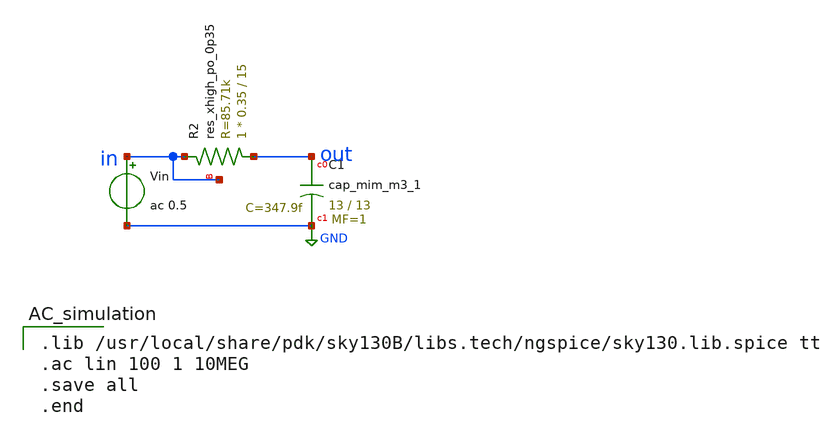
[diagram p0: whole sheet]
** sch_path: xschem/analog_desing/Filtro/LowPassFilter.sch
**.subckt LowPassFilter
XC1 out GND sky130_fd_pr__cap_mim_m3_1 W=13 L=13 MF=1 m=1
Vin in GND ac 0.5
XR2 out in in sky130_fd_pr__res_xhigh_po_0p35 L=15 mult=1 m=1
**** begin user architecture code

.lib /usr/local/share/pdk/sky130B/libs.tech/ngspice/sky130.lib.spice tt
.ac lin 100 1 10MEG
.save all
.end

**** end user architecture code
**.ends
.GLOBAL GND
.end
